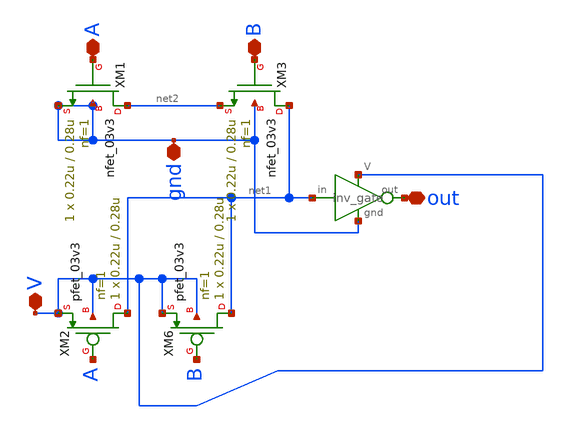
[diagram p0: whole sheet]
** sch_path: xschem/and_gate.sch
**.subckt and_gate A out gnd V B
*.iopin A
*.iopin out
*.iopin gnd
*.iopin V
*.iopin B
X1 V gnd net1 out inv_gate
XM6 net1 B V V pfet_03v3 L=0.28u W=0.22u nf=1 ad='int((nf+1)/2) * W/nf * 0.18u' as='int((nf+2)/2) * W/nf * 0.18u'
+ pd='2*int((nf+1)/2) * (W/nf + 0.18u)' ps='2*int((nf+2)/2) * (W/nf + 0.18u)' nrd='0.18u / W' nrs='0.18u / W'
+ sa=0 sb=0 sd=0 m=1
XM1 net2 A gnd gnd nfet_03v3 L=0.28u W=0.22u nf=1 ad='int((nf+1)/2) * W/nf * 0.18u' as='int((nf+2)/2) * W/nf * 0.18u'
+ pd='2*int((nf+1)/2) * (W/nf + 0.18u)' ps='2*int((nf+2)/2) * (W/nf + 0.18u)' nrd='0.18u / W' nrs='0.18u / W'
+ sa=0 sb=0 sd=0 m=1
XM3 net1 B net2 gnd nfet_03v3 L=0.28u W=0.22u nf=1 ad='int((nf+1)/2) * W/nf * 0.18u' as='int((nf+2)/2) * W/nf * 0.18u'
+ pd='2*int((nf+1)/2) * (W/nf + 0.18u)' ps='2*int((nf+2)/2) * (W/nf + 0.18u)' nrd='0.18u / W' nrs='0.18u / W'
+ sa=0 sb=0 sd=0 m=1
XM2 net1 A V V pfet_03v3 L=0.28u W=0.22u nf=1 ad='int((nf+1)/2) * W/nf * 0.18u' as='int((nf+2)/2) * W/nf * 0.18u'
+ pd='2*int((nf+1)/2) * (W/nf + 0.18u)' ps='2*int((nf+2)/2) * (W/nf + 0.18u)' nrd='0.18u / W' nrs='0.18u / W'
+ sa=0 sb=0 sd=0 m=1
**.ends

* expanding   symbol:  inv_gate.sym # of pins=4
** sym_path: inv_gate.sym
** sch_path: inv_gate.sch
.subckt inv_gate V gnd in out
*.iopin in
*.iopin out
*.iopin gnd
*.iopin V
XM3 out in gnd gnd nfet_03v3 L=0.28u W=0.22u nf=1 ad='int((nf+1)/2) * W/nf * 0.18u' as='int((nf+2)/2) * W/nf * 0.18u'
+ pd='2*int((nf+1)/2) * (W/nf + 0.18u)' ps='2*int((nf+2)/2) * (W/nf + 0.18u)' nrd='0.18u / W' nrs='0.18u / W'
+ sa=0 sb=0 sd=0 m=1
XM4 out in V V pfet_03v3 L=0.28u W=0.22u nf=1 ad='int((nf+1)/2) * W/nf * 0.18u' as='int((nf+2)/2) * W/nf * 0.18u'
+ pd='2*int((nf+1)/2) * (W/nf + 0.18u)' ps='2*int((nf+2)/2) * (W/nf + 0.18u)' nrd='0.18u / W' nrs='0.18u / W'
+ sa=0 sb=0 sd=0 m=1
.ends

.end
